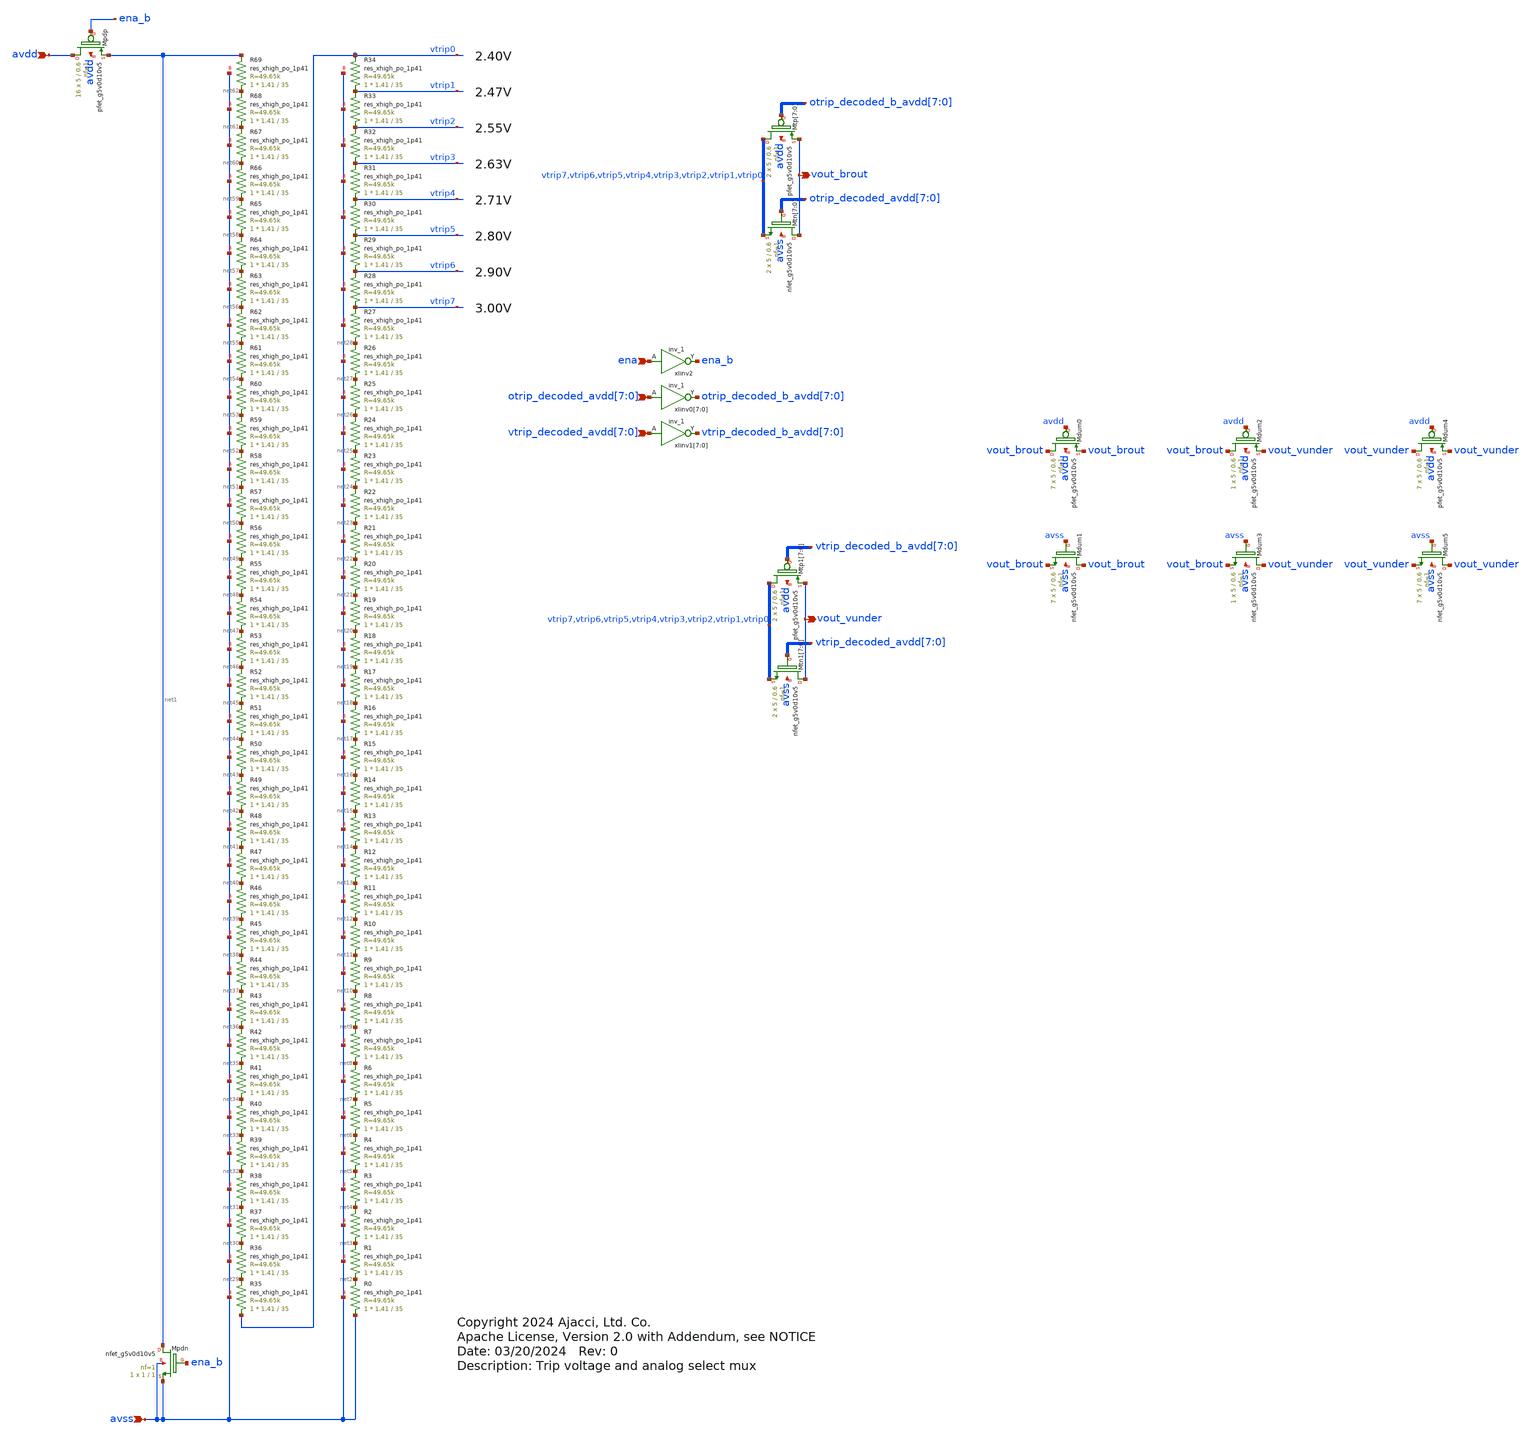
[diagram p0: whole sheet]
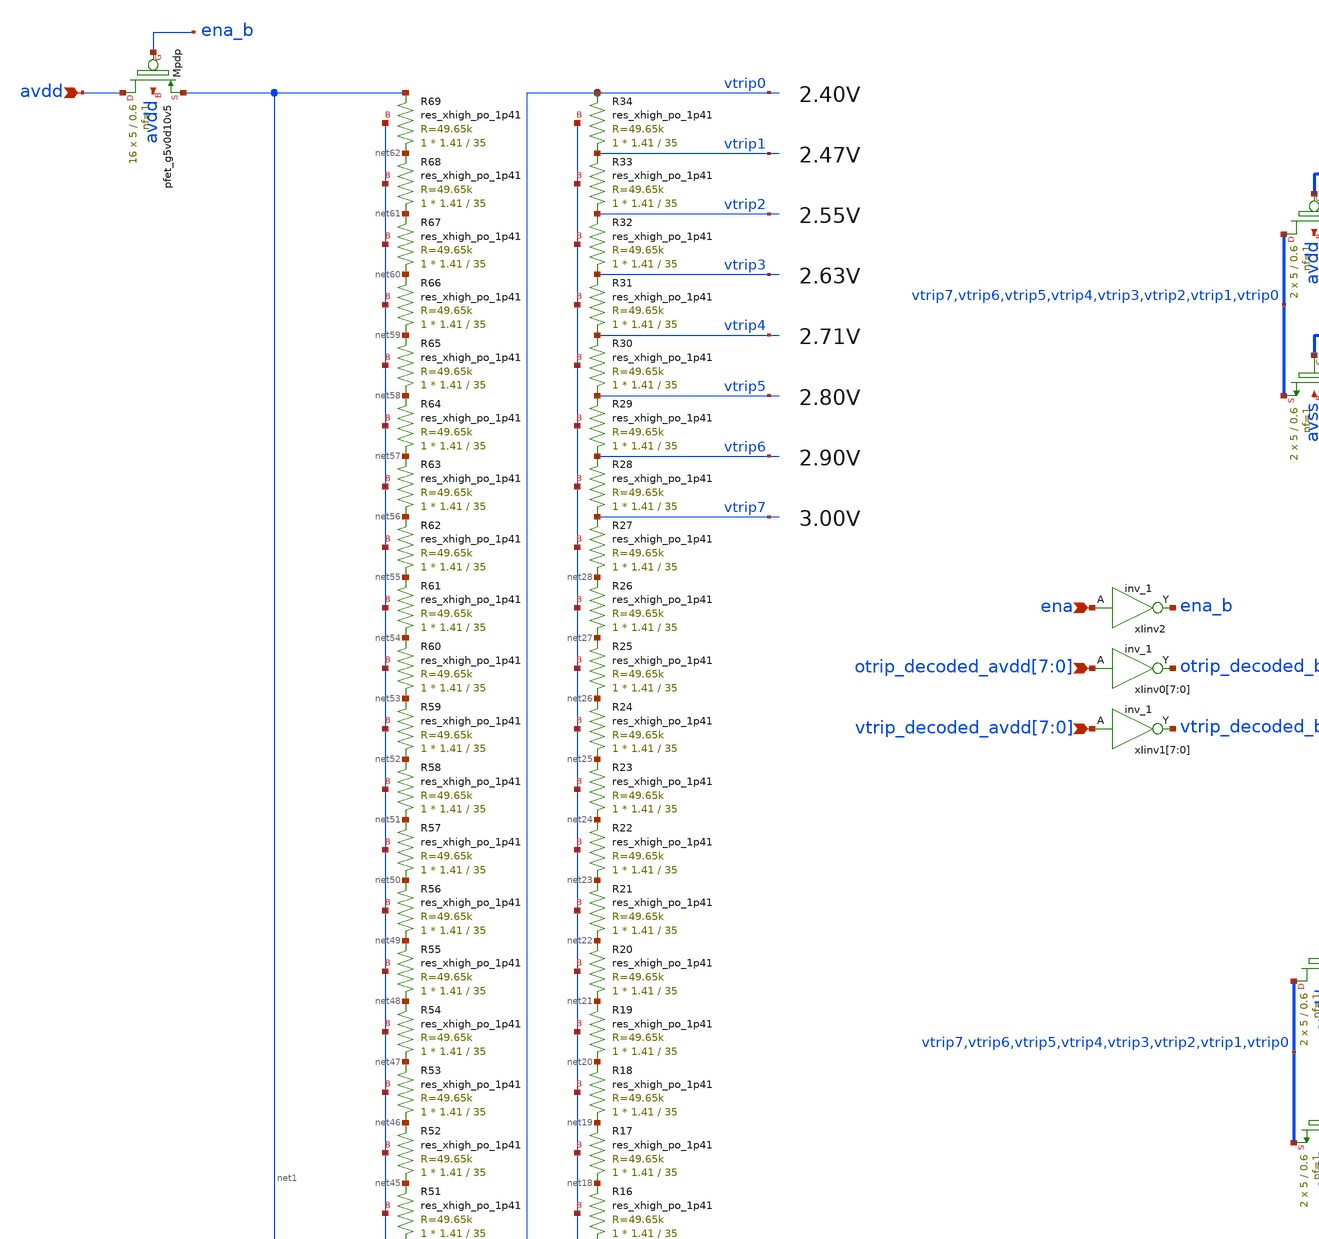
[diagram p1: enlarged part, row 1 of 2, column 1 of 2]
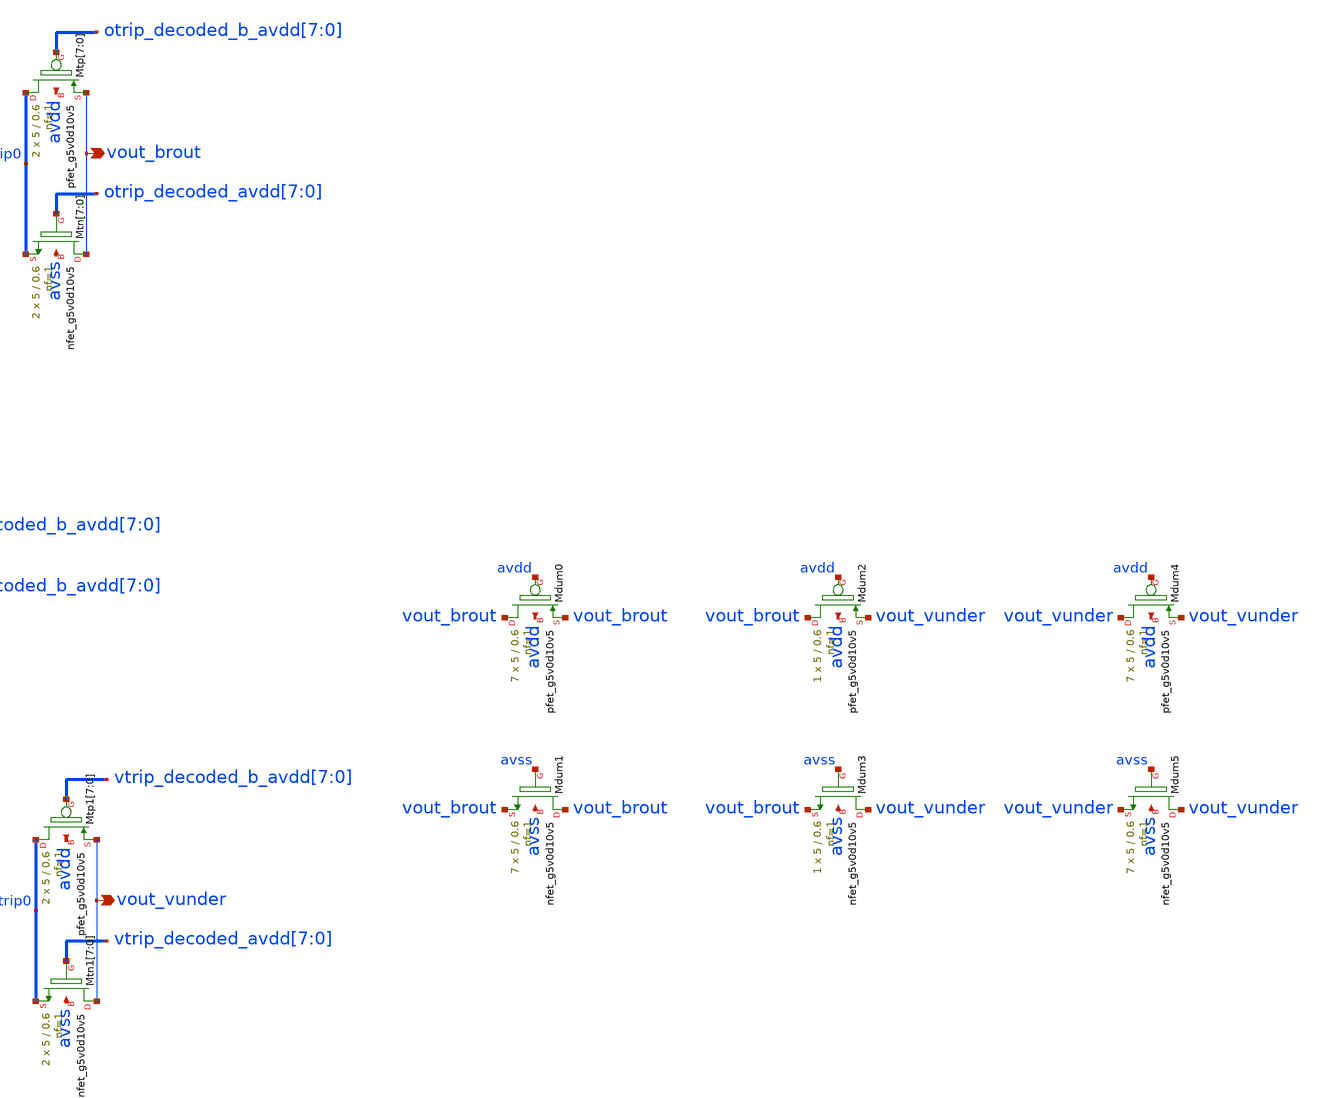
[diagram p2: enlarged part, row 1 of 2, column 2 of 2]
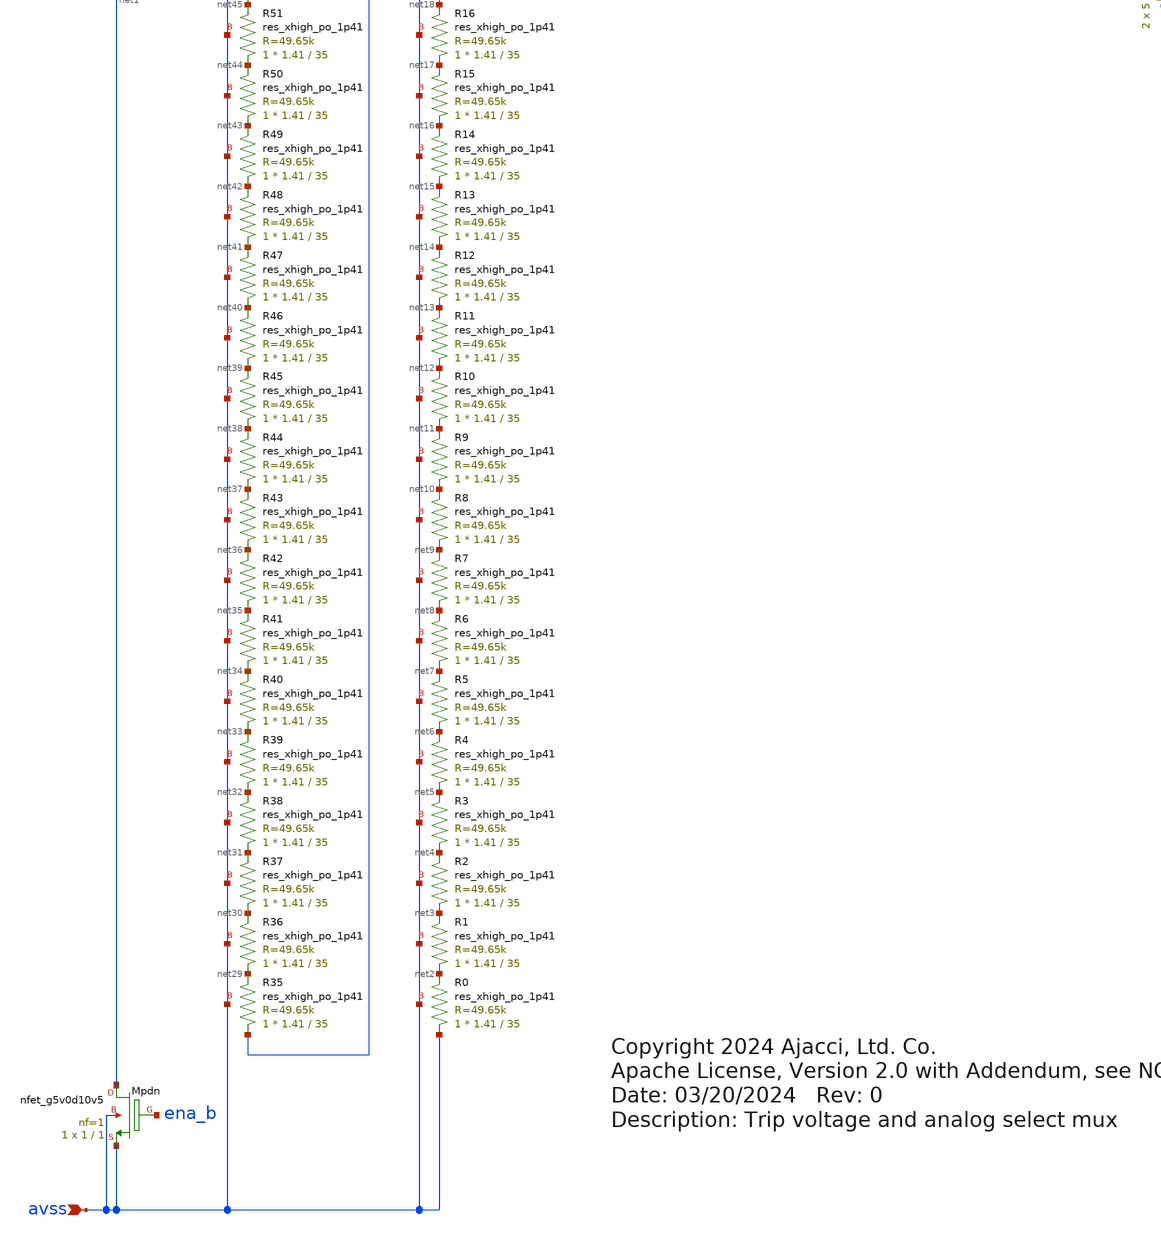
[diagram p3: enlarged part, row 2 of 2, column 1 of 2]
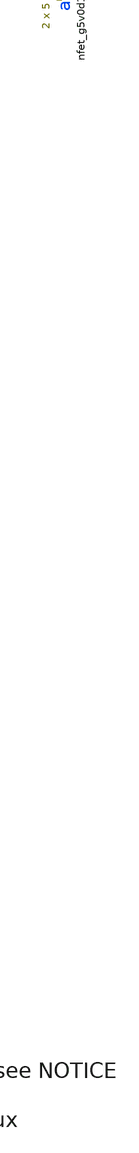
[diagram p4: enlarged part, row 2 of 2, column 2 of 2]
** sch_path: xschem/rstring_mux.sch
* Copyright 2024 Ajacci, Ltd. Co.
* Apache License, Version 2.0 with Addendum, see NOTICE
**.subckt rstring_mux vout_brout
*+ otrip_decoded_avdd[7],otrip_decoded_avdd[6],otrip_decoded_avdd[5],otrip_decoded_avdd[4],otrip_decoded_avdd[3],otrip_decoded_avdd[2],otrip_decoded_avdd[1],otrip_decoded_avdd[0] vout_vunder
*+ vtrip_decoded_avdd[7],vtrip_decoded_avdd[6],vtrip_decoded_avdd[5],vtrip_decoded_avdd[4],vtrip_decoded_avdd[3],vtrip_decoded_avdd[2],vtrip_decoded_avdd[1],vtrip_decoded_avdd[0] ena avdd avss
*.opin vout_brout
*.ipin
*+ otrip_decoded_avdd[7],otrip_decoded_avdd[6],otrip_decoded_avdd[5],otrip_decoded_avdd[4],otrip_decoded_avdd[3],otrip_decoded_avdd[2],otrip_decoded_avdd[1],otrip_decoded_avdd[0]
*.opin vout_vunder
*.ipin
*+ vtrip_decoded_avdd[7],vtrip_decoded_avdd[6],vtrip_decoded_avdd[5],vtrip_decoded_avdd[4],vtrip_decoded_avdd[3],vtrip_decoded_avdd[2],vtrip_decoded_avdd[1],vtrip_decoded_avdd[0]
*.ipin ena
*.ipin avdd
*.ipin avss
XR1 net2 net3 avss sky130_fd_pr__res_xhigh_po_1p41 L=35 mult=1 m=1
XR2 net3 net4 avss sky130_fd_pr__res_xhigh_po_1p41 L=35 mult=1 m=1
XR0 avss net2 avss sky130_fd_pr__res_xhigh_po_1p41 L=35 mult=1 m=1
XR3 net4 net5 avss sky130_fd_pr__res_xhigh_po_1p41 L=35 mult=1 m=1
XR4 net5 net6 avss sky130_fd_pr__res_xhigh_po_1p41 L=35 mult=1 m=1
XR5 net6 net7 avss sky130_fd_pr__res_xhigh_po_1p41 L=35 mult=1 m=1
XR6 net7 net8 avss sky130_fd_pr__res_xhigh_po_1p41 L=35 mult=1 m=1
XR7 net8 net9 avss sky130_fd_pr__res_xhigh_po_1p41 L=35 mult=1 m=1
XR8 net9 net10 avss sky130_fd_pr__res_xhigh_po_1p41 L=35 mult=1 m=1
XR9 net10 net11 avss sky130_fd_pr__res_xhigh_po_1p41 L=35 mult=1 m=1
XR10 net11 net12 avss sky130_fd_pr__res_xhigh_po_1p41 L=35 mult=1 m=1
XR11 net12 net13 avss sky130_fd_pr__res_xhigh_po_1p41 L=35 mult=1 m=1
XR12 net13 net14 avss sky130_fd_pr__res_xhigh_po_1p41 L=35 mult=1 m=1
XR13 net14 net15 avss sky130_fd_pr__res_xhigh_po_1p41 L=35 mult=1 m=1
XR14 net15 net16 avss sky130_fd_pr__res_xhigh_po_1p41 L=35 mult=1 m=1
XR15 net16 net17 avss sky130_fd_pr__res_xhigh_po_1p41 L=35 mult=1 m=1
XR16 net17 net18 avss sky130_fd_pr__res_xhigh_po_1p41 L=35 mult=1 m=1
XR17 net18 net19 avss sky130_fd_pr__res_xhigh_po_1p41 L=35 mult=1 m=1
XR18 net19 net20 avss sky130_fd_pr__res_xhigh_po_1p41 L=35 mult=1 m=1
XR19 net20 net21 avss sky130_fd_pr__res_xhigh_po_1p41 L=35 mult=1 m=1
XR20 net21 net22 avss sky130_fd_pr__res_xhigh_po_1p41 L=35 mult=1 m=1
XR21 net22 net23 avss sky130_fd_pr__res_xhigh_po_1p41 L=35 mult=1 m=1
XR22 net23 net24 avss sky130_fd_pr__res_xhigh_po_1p41 L=35 mult=1 m=1
XR23 net24 net25 avss sky130_fd_pr__res_xhigh_po_1p41 L=35 mult=1 m=1
XR24 net25 net26 avss sky130_fd_pr__res_xhigh_po_1p41 L=35 mult=1 m=1
XR25 net26 net27 avss sky130_fd_pr__res_xhigh_po_1p41 L=35 mult=1 m=1
XR26 net27 net28 avss sky130_fd_pr__res_xhigh_po_1p41 L=35 mult=1 m=1
XR27 net28 vtrip7 avss sky130_fd_pr__res_xhigh_po_1p41 L=35 mult=1 m=1
XR28 vtrip7 vtrip6 avss sky130_fd_pr__res_xhigh_po_1p41 L=35 mult=1 m=1
XR29 vtrip6 vtrip5 avss sky130_fd_pr__res_xhigh_po_1p41 L=35 mult=1 m=1
XR30 vtrip5 vtrip4 avss sky130_fd_pr__res_xhigh_po_1p41 L=35 mult=1 m=1
XR31 vtrip4 vtrip3 avss sky130_fd_pr__res_xhigh_po_1p41 L=35 mult=1 m=1
XR32 vtrip3 vtrip2 avss sky130_fd_pr__res_xhigh_po_1p41 L=35 mult=1 m=1
XR33 vtrip2 vtrip1 avss sky130_fd_pr__res_xhigh_po_1p41 L=35 mult=1 m=1
XR34 vtrip1 vtrip0 avss sky130_fd_pr__res_xhigh_po_1p41 L=35 mult=1 m=1
XR35 vtrip0 net29 avss sky130_fd_pr__res_xhigh_po_1p41 L=35 mult=1 m=1
XR36 net29 net30 avss sky130_fd_pr__res_xhigh_po_1p41 L=35 mult=1 m=1
XR37 net30 net31 avss sky130_fd_pr__res_xhigh_po_1p41 L=35 mult=1 m=1
XR38 net31 net32 avss sky130_fd_pr__res_xhigh_po_1p41 L=35 mult=1 m=1
XR39 net32 net33 avss sky130_fd_pr__res_xhigh_po_1p41 L=35 mult=1 m=1
XR40 net33 net34 avss sky130_fd_pr__res_xhigh_po_1p41 L=35 mult=1 m=1
XR41 net34 net35 avss sky130_fd_pr__res_xhigh_po_1p41 L=35 mult=1 m=1
XR42 net35 net36 avss sky130_fd_pr__res_xhigh_po_1p41 L=35 mult=1 m=1
XR43 net36 net37 avss sky130_fd_pr__res_xhigh_po_1p41 L=35 mult=1 m=1
XR44 net37 net38 avss sky130_fd_pr__res_xhigh_po_1p41 L=35 mult=1 m=1
XR45 net38 net39 avss sky130_fd_pr__res_xhigh_po_1p41 L=35 mult=1 m=1
XR46 net39 net40 avss sky130_fd_pr__res_xhigh_po_1p41 L=35 mult=1 m=1
XR47 net40 net41 avss sky130_fd_pr__res_xhigh_po_1p41 L=35 mult=1 m=1
XR48 net41 net42 avss sky130_fd_pr__res_xhigh_po_1p41 L=35 mult=1 m=1
XR49 net42 net43 avss sky130_fd_pr__res_xhigh_po_1p41 L=35 mult=1 m=1
XR50 net43 net44 avss sky130_fd_pr__res_xhigh_po_1p41 L=35 mult=1 m=1
XR51 net44 net45 avss sky130_fd_pr__res_xhigh_po_1p41 L=35 mult=1 m=1
XR52 net45 net46 avss sky130_fd_pr__res_xhigh_po_1p41 L=35 mult=1 m=1
XR53 net46 net47 avss sky130_fd_pr__res_xhigh_po_1p41 L=35 mult=1 m=1
XR54 net47 net48 avss sky130_fd_pr__res_xhigh_po_1p41 L=35 mult=1 m=1
XR55 net48 net49 avss sky130_fd_pr__res_xhigh_po_1p41 L=35 mult=1 m=1
XR56 net49 net50 avss sky130_fd_pr__res_xhigh_po_1p41 L=35 mult=1 m=1
XR57 net50 net51 avss sky130_fd_pr__res_xhigh_po_1p41 L=35 mult=1 m=1
XR58 net51 net52 avss sky130_fd_pr__res_xhigh_po_1p41 L=35 mult=1 m=1
XR59 net52 net53 avss sky130_fd_pr__res_xhigh_po_1p41 L=35 mult=1 m=1
XR60 net53 net54 avss sky130_fd_pr__res_xhigh_po_1p41 L=35 mult=1 m=1
XR61 net54 net55 avss sky130_fd_pr__res_xhigh_po_1p41 L=35 mult=1 m=1
XR62 net55 net56 avss sky130_fd_pr__res_xhigh_po_1p41 L=35 mult=1 m=1
XR63 net56 net57 avss sky130_fd_pr__res_xhigh_po_1p41 L=35 mult=1 m=1
XR64 net57 net58 avss sky130_fd_pr__res_xhigh_po_1p41 L=35 mult=1 m=1
XR65 net58 net59 avss sky130_fd_pr__res_xhigh_po_1p41 L=35 mult=1 m=1
XR66 net59 net60 avss sky130_fd_pr__res_xhigh_po_1p41 L=35 mult=1 m=1
XR67 net60 net61 avss sky130_fd_pr__res_xhigh_po_1p41 L=35 mult=1 m=1
XR68 net61 net62 avss sky130_fd_pr__res_xhigh_po_1p41 L=35 mult=1 m=1
XR69 net62 net1 avss sky130_fd_pr__res_xhigh_po_1p41 L=35 mult=1 m=1
XMtp[7] vtrip7 otrip_decoded_b_avdd[7] vout_brout avdd sky130_fd_pr__pfet_g5v0d10v5 L=0.6 W=5 nf=1 ad='int((nf+1)/2) * W/nf * 0.29'
+ as='int((nf+2)/2) * W/nf * 0.29' pd='2*int((nf+1)/2) * (W/nf + 0.29)' ps='2*int((nf+2)/2) * (W/nf + 0.29)'
+ nrd='0.29 / W' nrs='0.29 / W' sa=0 sb=0 sd=0 mult=2 m=2
XMtp[6] vtrip6 otrip_decoded_b_avdd[6] vout_brout avdd sky130_fd_pr__pfet_g5v0d10v5 L=0.6 W=5 nf=1 ad='int((nf+1)/2) * W/nf * 0.29'
+ as='int((nf+2)/2) * W/nf * 0.29' pd='2*int((nf+1)/2) * (W/nf + 0.29)' ps='2*int((nf+2)/2) * (W/nf + 0.29)'
+ nrd='0.29 / W' nrs='0.29 / W' sa=0 sb=0 sd=0 mult=2 m=2
XMtp[5] vtrip5 otrip_decoded_b_avdd[5] vout_brout avdd sky130_fd_pr__pfet_g5v0d10v5 L=0.6 W=5 nf=1 ad='int((nf+1)/2) * W/nf * 0.29'
+ as='int((nf+2)/2) * W/nf * 0.29' pd='2*int((nf+1)/2) * (W/nf + 0.29)' ps='2*int((nf+2)/2) * (W/nf + 0.29)'
+ nrd='0.29 / W' nrs='0.29 / W' sa=0 sb=0 sd=0 mult=2 m=2
XMtp[4] vtrip4 otrip_decoded_b_avdd[4] vout_brout avdd sky130_fd_pr__pfet_g5v0d10v5 L=0.6 W=5 nf=1 ad='int((nf+1)/2) * W/nf * 0.29'
+ as='int((nf+2)/2) * W/nf * 0.29' pd='2*int((nf+1)/2) * (W/nf + 0.29)' ps='2*int((nf+2)/2) * (W/nf + 0.29)'
+ nrd='0.29 / W' nrs='0.29 / W' sa=0 sb=0 sd=0 mult=2 m=2
XMtp[3] vtrip3 otrip_decoded_b_avdd[3] vout_brout avdd sky130_fd_pr__pfet_g5v0d10v5 L=0.6 W=5 nf=1 ad='int((nf+1)/2) * W/nf * 0.29'
+ as='int((nf+2)/2) * W/nf * 0.29' pd='2*int((nf+1)/2) * (W/nf + 0.29)' ps='2*int((nf+2)/2) * (W/nf + 0.29)'
+ nrd='0.29 / W' nrs='0.29 / W' sa=0 sb=0 sd=0 mult=2 m=2
XMtp[2] vtrip2 otrip_decoded_b_avdd[2] vout_brout avdd sky130_fd_pr__pfet_g5v0d10v5 L=0.6 W=5 nf=1 ad='int((nf+1)/2) * W/nf * 0.29'
+ as='int((nf+2)/2) * W/nf * 0.29' pd='2*int((nf+1)/2) * (W/nf + 0.29)' ps='2*int((nf+2)/2) * (W/nf + 0.29)'
+ nrd='0.29 / W' nrs='0.29 / W' sa=0 sb=0 sd=0 mult=2 m=2
XMtp[1] vtrip1 otrip_decoded_b_avdd[1] vout_brout avdd sky130_fd_pr__pfet_g5v0d10v5 L=0.6 W=5 nf=1 ad='int((nf+1)/2) * W/nf * 0.29'
+ as='int((nf+2)/2) * W/nf * 0.29' pd='2*int((nf+1)/2) * (W/nf + 0.29)' ps='2*int((nf+2)/2) * (W/nf + 0.29)'
+ nrd='0.29 / W' nrs='0.29 / W' sa=0 sb=0 sd=0 mult=2 m=2
XMtp[0] vtrip0 otrip_decoded_b_avdd[0] vout_brout avdd sky130_fd_pr__pfet_g5v0d10v5 L=0.6 W=5 nf=1 ad='int((nf+1)/2) * W/nf * 0.29'
+ as='int((nf+2)/2) * W/nf * 0.29' pd='2*int((nf+1)/2) * (W/nf + 0.29)' ps='2*int((nf+2)/2) * (W/nf + 0.29)'
+ nrd='0.29 / W' nrs='0.29 / W' sa=0 sb=0 sd=0 mult=2 m=2
XMtn[7] vout_brout otrip_decoded_avdd[7] vtrip7 avss sky130_fd_pr__nfet_g5v0d10v5 L=0.6 W=5 nf=1 ad='int((nf+1)/2) * W/nf * 0.29'
+ as='int((nf+2)/2) * W/nf * 0.29' pd='2*int((nf+1)/2) * (W/nf + 0.29)' ps='2*int((nf+2)/2) * (W/nf + 0.29)'
+ nrd='0.29 / W' nrs='0.29 / W' sa=0 sb=0 sd=0 mult=2 m=2
XMtn[6] vout_brout otrip_decoded_avdd[6] vtrip6 avss sky130_fd_pr__nfet_g5v0d10v5 L=0.6 W=5 nf=1 ad='int((nf+1)/2) * W/nf * 0.29'
+ as='int((nf+2)/2) * W/nf * 0.29' pd='2*int((nf+1)/2) * (W/nf + 0.29)' ps='2*int((nf+2)/2) * (W/nf + 0.29)'
+ nrd='0.29 / W' nrs='0.29 / W' sa=0 sb=0 sd=0 mult=2 m=2
XMtn[5] vout_brout otrip_decoded_avdd[5] vtrip5 avss sky130_fd_pr__nfet_g5v0d10v5 L=0.6 W=5 nf=1 ad='int((nf+1)/2) * W/nf * 0.29'
+ as='int((nf+2)/2) * W/nf * 0.29' pd='2*int((nf+1)/2) * (W/nf + 0.29)' ps='2*int((nf+2)/2) * (W/nf + 0.29)'
+ nrd='0.29 / W' nrs='0.29 / W' sa=0 sb=0 sd=0 mult=2 m=2
XMtn[4] vout_brout otrip_decoded_avdd[4] vtrip4 avss sky130_fd_pr__nfet_g5v0d10v5 L=0.6 W=5 nf=1 ad='int((nf+1)/2) * W/nf * 0.29'
+ as='int((nf+2)/2) * W/nf * 0.29' pd='2*int((nf+1)/2) * (W/nf + 0.29)' ps='2*int((nf+2)/2) * (W/nf + 0.29)'
+ nrd='0.29 / W' nrs='0.29 / W' sa=0 sb=0 sd=0 mult=2 m=2
XMtn[3] vout_brout otrip_decoded_avdd[3] vtrip3 avss sky130_fd_pr__nfet_g5v0d10v5 L=0.6 W=5 nf=1 ad='int((nf+1)/2) * W/nf * 0.29'
+ as='int((nf+2)/2) * W/nf * 0.29' pd='2*int((nf+1)/2) * (W/nf + 0.29)' ps='2*int((nf+2)/2) * (W/nf + 0.29)'
+ nrd='0.29 / W' nrs='0.29 / W' sa=0 sb=0 sd=0 mult=2 m=2
XMtn[2] vout_brout otrip_decoded_avdd[2] vtrip2 avss sky130_fd_pr__nfet_g5v0d10v5 L=0.6 W=5 nf=1 ad='int((nf+1)/2) * W/nf * 0.29'
+ as='int((nf+2)/2) * W/nf * 0.29' pd='2*int((nf+1)/2) * (W/nf + 0.29)' ps='2*int((nf+2)/2) * (W/nf + 0.29)'
+ nrd='0.29 / W' nrs='0.29 / W' sa=0 sb=0 sd=0 mult=2 m=2
XMtn[1] vout_brout otrip_decoded_avdd[1] vtrip1 avss sky130_fd_pr__nfet_g5v0d10v5 L=0.6 W=5 nf=1 ad='int((nf+1)/2) * W/nf * 0.29'
+ as='int((nf+2)/2) * W/nf * 0.29' pd='2*int((nf+1)/2) * (W/nf + 0.29)' ps='2*int((nf+2)/2) * (W/nf + 0.29)'
+ nrd='0.29 / W' nrs='0.29 / W' sa=0 sb=0 sd=0 mult=2 m=2
XMtn[0] vout_brout otrip_decoded_avdd[0] vtrip0 avss sky130_fd_pr__nfet_g5v0d10v5 L=0.6 W=5 nf=1 ad='int((nf+1)/2) * W/nf * 0.29'
+ as='int((nf+2)/2) * W/nf * 0.29' pd='2*int((nf+1)/2) * (W/nf + 0.29)' ps='2*int((nf+2)/2) * (W/nf + 0.29)'
+ nrd='0.29 / W' nrs='0.29 / W' sa=0 sb=0 sd=0 mult=2 m=2
XMtp1[7] vtrip7 vtrip_decoded_b_avdd[7] vout_vunder avdd sky130_fd_pr__pfet_g5v0d10v5 L=0.6 W=5 nf=1
+ ad='int((nf+1)/2) * W/nf * 0.29' as='int((nf+2)/2) * W/nf * 0.29' pd='2*int((nf+1)/2) * (W/nf + 0.29)'
+ ps='2*int((nf+2)/2) * (W/nf + 0.29)' nrd='0.29 / W' nrs='0.29 / W' sa=0 sb=0 sd=0 mult=2 m=2
XMtp1[6] vtrip6 vtrip_decoded_b_avdd[6] vout_vunder avdd sky130_fd_pr__pfet_g5v0d10v5 L=0.6 W=5 nf=1
+ ad='int((nf+1)/2) * W/nf * 0.29' as='int((nf+2)/2) * W/nf * 0.29' pd='2*int((nf+1)/2) * (W/nf + 0.29)'
+ ps='2*int((nf+2)/2) * (W/nf + 0.29)' nrd='0.29 / W' nrs='0.29 / W' sa=0 sb=0 sd=0 mult=2 m=2
XMtp1[5] vtrip5 vtrip_decoded_b_avdd[5] vout_vunder avdd sky130_fd_pr__pfet_g5v0d10v5 L=0.6 W=5 nf=1
+ ad='int((nf+1)/2) * W/nf * 0.29' as='int((nf+2)/2) * W/nf * 0.29' pd='2*int((nf+1)/2) * (W/nf + 0.29)'
+ ps='2*int((nf+2)/2) * (W/nf + 0.29)' nrd='0.29 / W' nrs='0.29 / W' sa=0 sb=0 sd=0 mult=2 m=2
XMtp1[4] vtrip4 vtrip_decoded_b_avdd[4] vout_vunder avdd sky130_fd_pr__pfet_g5v0d10v5 L=0.6 W=5 nf=1
+ ad='int((nf+1)/2) * W/nf * 0.29' as='int((nf+2)/2) * W/nf * 0.29' pd='2*int((nf+1)/2) * (W/nf + 0.29)'
+ ps='2*int((nf+2)/2) * (W/nf + 0.29)' nrd='0.29 / W' nrs='0.29 / W' sa=0 sb=0 sd=0 mult=2 m=2
XMtp1[3] vtrip3 vtrip_decoded_b_avdd[3] vout_vunder avdd sky130_fd_pr__pfet_g5v0d10v5 L=0.6 W=5 nf=1
+ ad='int((nf+1)/2) * W/nf * 0.29' as='int((nf+2)/2) * W/nf * 0.29' pd='2*int((nf+1)/2) * (W/nf + 0.29)'
+ ps='2*int((nf+2)/2) * (W/nf + 0.29)' nrd='0.29 / W' nrs='0.29 / W' sa=0 sb=0 sd=0 mult=2 m=2
XMtp1[2] vtrip2 vtrip_decoded_b_avdd[2] vout_vunder avdd sky130_fd_pr__pfet_g5v0d10v5 L=0.6 W=5 nf=1
+ ad='int((nf+1)/2) * W/nf * 0.29' as='int((nf+2)/2) * W/nf * 0.29' pd='2*int((nf+1)/2) * (W/nf + 0.29)'
+ ps='2*int((nf+2)/2) * (W/nf + 0.29)' nrd='0.29 / W' nrs='0.29 / W' sa=0 sb=0 sd=0 mult=2 m=2
XMtp1[1] vtrip1 vtrip_decoded_b_avdd[1] vout_vunder avdd sky130_fd_pr__pfet_g5v0d10v5 L=0.6 W=5 nf=1
+ ad='int((nf+1)/2) * W/nf * 0.29' as='int((nf+2)/2) * W/nf * 0.29' pd='2*int((nf+1)/2) * (W/nf + 0.29)'
+ ps='2*int((nf+2)/2) * (W/nf + 0.29)' nrd='0.29 / W' nrs='0.29 / W' sa=0 sb=0 sd=0 mult=2 m=2
XMtp1[0] vtrip0 vtrip_decoded_b_avdd[0] vout_vunder avdd sky130_fd_pr__pfet_g5v0d10v5 L=0.6 W=5 nf=1
+ ad='int((nf+1)/2) * W/nf * 0.29' as='int((nf+2)/2) * W/nf * 0.29' pd='2*int((nf+1)/2) * (W/nf + 0.29)'
+ ps='2*int((nf+2)/2) * (W/nf + 0.29)' nrd='0.29 / W' nrs='0.29 / W' sa=0 sb=0 sd=0 mult=2 m=2
XMtn1[7] vout_vunder vtrip_decoded_avdd[7] vtrip7 avss sky130_fd_pr__nfet_g5v0d10v5 L=0.6 W=5 nf=1 ad='int((nf+1)/2) * W/nf * 0.29'
+ as='int((nf+2)/2) * W/nf * 0.29' pd='2*int((nf+1)/2) * (W/nf + 0.29)' ps='2*int((nf+2)/2) * (W/nf + 0.29)'
+ nrd='0.29 / W' nrs='0.29 / W' sa=0 sb=0 sd=0 mult=2 m=2
XMtn1[6] vout_vunder vtrip_decoded_avdd[6] vtrip6 avss sky130_fd_pr__nfet_g5v0d10v5 L=0.6 W=5 nf=1 ad='int((nf+1)/2) * W/nf * 0.29'
+ as='int((nf+2)/2) * W/nf * 0.29' pd='2*int((nf+1)/2) * (W/nf + 0.29)' ps='2*int((nf+2)/2) * (W/nf + 0.29)'
+ nrd='0.29 / W' nrs='0.29 / W' sa=0 sb=0 sd=0 mult=2 m=2
XMtn1[5] vout_vunder vtrip_decoded_avdd[5] vtrip5 avss sky130_fd_pr__nfet_g5v0d10v5 L=0.6 W=5 nf=1 ad='int((nf+1)/2) * W/nf * 0.29'
+ as='int((nf+2)/2) * W/nf * 0.29' pd='2*int((nf+1)/2) * (W/nf + 0.29)' ps='2*int((nf+2)/2) * (W/nf + 0.29)'
+ nrd='0.29 / W' nrs='0.29 / W' sa=0 sb=0 sd=0 mult=2 m=2
XMtn1[4] vout_vunder vtrip_decoded_avdd[4] vtrip4 avss sky130_fd_pr__nfet_g5v0d10v5 L=0.6 W=5 nf=1 ad='int((nf+1)/2) * W/nf * 0.29'
+ as='int((nf+2)/2) * W/nf * 0.29' pd='2*int((nf+1)/2) * (W/nf + 0.29)' ps='2*int((nf+2)/2) * (W/nf + 0.29)'
+ nrd='0.29 / W' nrs='0.29 / W' sa=0 sb=0 sd=0 mult=2 m=2
XMtn1[3] vout_vunder vtrip_decoded_avdd[3] vtrip3 avss sky130_fd_pr__nfet_g5v0d10v5 L=0.6 W=5 nf=1 ad='int((nf+1)/2) * W/nf * 0.29'
+ as='int((nf+2)/2) * W/nf * 0.29' pd='2*int((nf+1)/2) * (W/nf + 0.29)' ps='2*int((nf+2)/2) * (W/nf + 0.29)'
+ nrd='0.29 / W' nrs='0.29 / W' sa=0 sb=0 sd=0 mult=2 m=2
XMtn1[2] vout_vunder vtrip_decoded_avdd[2] vtrip2 avss sky130_fd_pr__nfet_g5v0d10v5 L=0.6 W=5 nf=1 ad='int((nf+1)/2) * W/nf * 0.29'
+ as='int((nf+2)/2) * W/nf * 0.29' pd='2*int((nf+1)/2) * (W/nf + 0.29)' ps='2*int((nf+2)/2) * (W/nf + 0.29)'
+ nrd='0.29 / W' nrs='0.29 / W' sa=0 sb=0 sd=0 mult=2 m=2
XMtn1[1] vout_vunder vtrip_decoded_avdd[1] vtrip1 avss sky130_fd_pr__nfet_g5v0d10v5 L=0.6 W=5 nf=1 ad='int((nf+1)/2) * W/nf * 0.29'
+ as='int((nf+2)/2) * W/nf * 0.29' pd='2*int((nf+1)/2) * (W/nf + 0.29)' ps='2*int((nf+2)/2) * (W/nf + 0.29)'
+ nrd='0.29 / W' nrs='0.29 / W' sa=0 sb=0 sd=0 mult=2 m=2
XMtn1[0] vout_vunder vtrip_decoded_avdd[0] vtrip0 avss sky130_fd_pr__nfet_g5v0d10v5 L=0.6 W=5 nf=1 ad='int((nf+1)/2) * W/nf * 0.29'
+ as='int((nf+2)/2) * W/nf * 0.29' pd='2*int((nf+1)/2) * (W/nf + 0.29)' ps='2*int((nf+2)/2) * (W/nf + 0.29)'
+ nrd='0.29 / W' nrs='0.29 / W' sa=0 sb=0 sd=0 mult=2 m=2
xIinv0[7] otrip_decoded_avdd[7] avss avss avdd avdd otrip_decoded_b_avdd[7] sky130_fd_sc_hvl__inv_1
xIinv0[6] otrip_decoded_avdd[6] avss avss avdd avdd otrip_decoded_b_avdd[6] sky130_fd_sc_hvl__inv_1
xIinv0[5] otrip_decoded_avdd[5] avss avss avdd avdd otrip_decoded_b_avdd[5] sky130_fd_sc_hvl__inv_1
xIinv0[4] otrip_decoded_avdd[4] avss avss avdd avdd otrip_decoded_b_avdd[4] sky130_fd_sc_hvl__inv_1
xIinv0[3] otrip_decoded_avdd[3] avss avss avdd avdd otrip_decoded_b_avdd[3] sky130_fd_sc_hvl__inv_1
xIinv0[2] otrip_decoded_avdd[2] avss avss avdd avdd otrip_decoded_b_avdd[2] sky130_fd_sc_hvl__inv_1
xIinv0[1] otrip_decoded_avdd[1] avss avss avdd avdd otrip_decoded_b_avdd[1] sky130_fd_sc_hvl__inv_1
xIinv0[0] otrip_decoded_avdd[0] avss avss avdd avdd otrip_decoded_b_avdd[0] sky130_fd_sc_hvl__inv_1
xIinv1[7] vtrip_decoded_avdd[7] avss avss avdd avdd vtrip_decoded_b_avdd[7] sky130_fd_sc_hvl__inv_1
xIinv1[6] vtrip_decoded_avdd[6] avss avss avdd avdd vtrip_decoded_b_avdd[6] sky130_fd_sc_hvl__inv_1
xIinv1[5] vtrip_decoded_avdd[5] avss avss avdd avdd vtrip_decoded_b_avdd[5] sky130_fd_sc_hvl__inv_1
xIinv1[4] vtrip_decoded_avdd[4] avss avss avdd avdd vtrip_decoded_b_avdd[4] sky130_fd_sc_hvl__inv_1
xIinv1[3] vtrip_decoded_avdd[3] avss avss avdd avdd vtrip_decoded_b_avdd[3] sky130_fd_sc_hvl__inv_1
xIinv1[2] vtrip_decoded_avdd[2] avss avss avdd avdd vtrip_decoded_b_avdd[2] sky130_fd_sc_hvl__inv_1
xIinv1[1] vtrip_decoded_avdd[1] avss avss avdd avdd vtrip_decoded_b_avdd[1] sky130_fd_sc_hvl__inv_1
xIinv1[0] vtrip_decoded_avdd[0] avss avss avdd avdd vtrip_decoded_b_avdd[0] sky130_fd_sc_hvl__inv_1
xIinv2 ena avss avss avdd avdd ena_b sky130_fd_sc_hvl__inv_1
XMpdn net1 ena_b avss avss sky130_fd_pr__nfet_g5v0d10v5 L=1 W=1 nf=1 ad='int((nf+1)/2) * W/nf * 0.29'
+ as='int((nf+2)/2) * W/nf * 0.29' pd='2*int((nf+1)/2) * (W/nf + 0.29)' ps='2*int((nf+2)/2) * (W/nf + 0.29)'
+ nrd='0.29 / W' nrs='0.29 / W' sa=0 sb=0 sd=0 mult=1 m=1
XMpdp avdd ena_b net1 avdd sky130_fd_pr__pfet_g5v0d10v5 L=0.6 W=5 nf=1 ad='int((nf+1)/2) * W/nf * 0.29'
+ as='int((nf+2)/2) * W/nf * 0.29' pd='2*int((nf+1)/2) * (W/nf + 0.29)' ps='2*int((nf+2)/2) * (W/nf + 0.29)'
+ nrd='0.29 / W' nrs='0.29 / W' sa=0 sb=0 sd=0 mult=16 m=16
XMdum0 vout_brout avdd vout_brout avdd sky130_fd_pr__pfet_g5v0d10v5 L=0.6 W=5 nf=1 ad='int((nf+1)/2) * W/nf * 0.29'
+ as='int((nf+2)/2) * W/nf * 0.29' pd='2*int((nf+1)/2) * (W/nf + 0.29)' ps='2*int((nf+2)/2) * (W/nf + 0.29)'
+ nrd='0.29 / W' nrs='0.29 / W' sa=0 sb=0 sd=0 mult=7 m=7
XMdum1 vout_brout avss vout_brout avss sky130_fd_pr__nfet_g5v0d10v5 L=0.6 W=5 nf=1 ad='int((nf+1)/2) * W/nf * 0.29'
+ as='int((nf+2)/2) * W/nf * 0.29' pd='2*int((nf+1)/2) * (W/nf + 0.29)' ps='2*int((nf+2)/2) * (W/nf + 0.29)'
+ nrd='0.29 / W' nrs='0.29 / W' sa=0 sb=0 sd=0 mult=7 m=7
XMdum2 vout_brout avdd vout_vunder avdd sky130_fd_pr__pfet_g5v0d10v5 L=0.6 W=5 nf=1 ad='int((nf+1)/2) * W/nf * 0.29'
+ as='int((nf+2)/2) * W/nf * 0.29' pd='2*int((nf+1)/2) * (W/nf + 0.29)' ps='2*int((nf+2)/2) * (W/nf + 0.29)'
+ nrd='0.29 / W' nrs='0.29 / W' sa=0 sb=0 sd=0 mult=1 m=1
XMdum3 vout_vunder avss vout_brout avss sky130_fd_pr__nfet_g5v0d10v5 L=0.6 W=5 nf=1 ad='int((nf+1)/2) * W/nf * 0.29'
+ as='int((nf+2)/2) * W/nf * 0.29' pd='2*int((nf+1)/2) * (W/nf + 0.29)' ps='2*int((nf+2)/2) * (W/nf + 0.29)'
+ nrd='0.29 / W' nrs='0.29 / W' sa=0 sb=0 sd=0 mult=1 m=1
XMdum4 vout_vunder avdd vout_vunder avdd sky130_fd_pr__pfet_g5v0d10v5 L=0.6 W=5 nf=1 ad='int((nf+1)/2) * W/nf * 0.29'
+ as='int((nf+2)/2) * W/nf * 0.29' pd='2*int((nf+1)/2) * (W/nf + 0.29)' ps='2*int((nf+2)/2) * (W/nf + 0.29)'
+ nrd='0.29 / W' nrs='0.29 / W' sa=0 sb=0 sd=0 mult=7 m=7
XMdum5 vout_vunder avss vout_vunder avss sky130_fd_pr__nfet_g5v0d10v5 L=0.6 W=5 nf=1 ad='int((nf+1)/2) * W/nf * 0.29'
+ as='int((nf+2)/2) * W/nf * 0.29' pd='2*int((nf+1)/2) * (W/nf + 0.29)' ps='2*int((nf+2)/2) * (W/nf + 0.29)'
+ nrd='0.29 / W' nrs='0.29 / W' sa=0 sb=0 sd=0 mult=7 m=7
**.ends
.end
